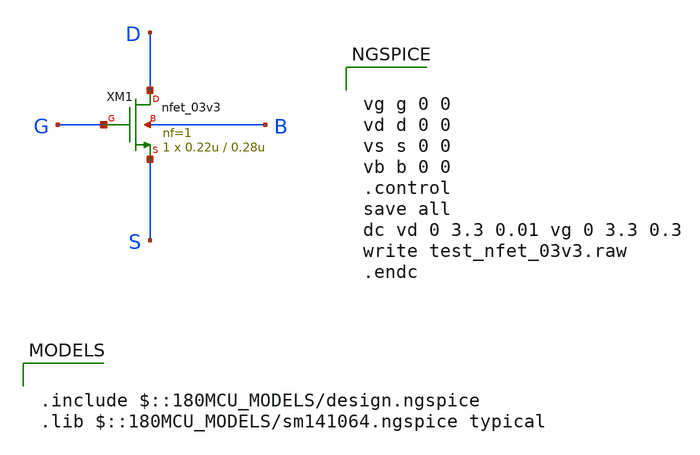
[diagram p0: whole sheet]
** sch_path: gf180mcuD/xschem_libs/gf180mcu_tests/test_nfet_03v3/schematic/test_nfet_03v3.sch
* Copyright 2022 GlobalFoundries PDK Authors
* Licensed under the Apache License, Version 2.0 (the "License");
* you may not use this file except in compliance with the License.
* You may obtain a copy of the License at
* https://www.apache.org/licenses/LICENSE-2.0
* Unless required by applicable law or agreed to in writing, software
* distributed under the License is distributed on an "AS IS" BASIS,
* WITHOUT WARRANTIES OR CONDITIONS OF ANY KIND, either express or implied.
* See the License for the specific language governing permissions and
* limitations under the License.
**.subckt test_nfet_03v3
XM1 D G S B nfet_03v3 L=0.28u W=0.22u nf=1 ad='int((nf+1)/2) * W/nf * 0.18u' as='int((nf+2)/2) * W/nf * 0.18u'
+ pd='2*int((nf+1)/2) * (W/nf + 0.18u)' ps='2*int((nf+2)/2) * (W/nf + 0.18u)' nrd='0.18u / W' nrs='0.18u / W'
+ sa=0 sb=0 sd=0 m=1
**** begin user architecture code

.include $::180MCU_MODELS/design.ngspice
.lib $::180MCU_MODELS/sm141064.ngspice typical



vg g 0 0
vd d 0 0
vs s 0 0
vb b 0 0
.control
save all
dc vd 0 3.3 0.01 vg 0 3.3 0.3
write test_nfet_03v3.raw
.endc


**** end user architecture code
**.ends
.end
